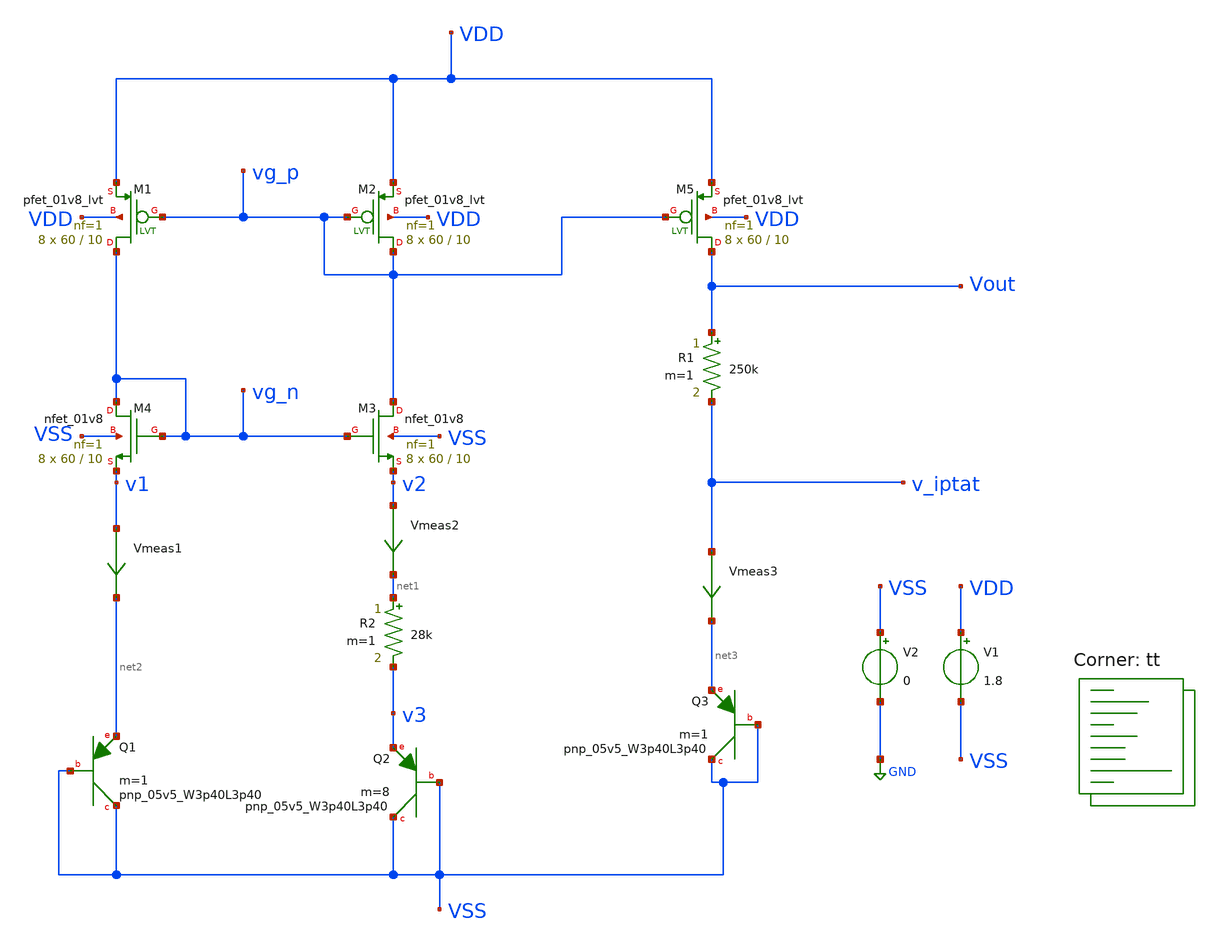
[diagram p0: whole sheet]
** sch_path: xschem/bandgap.sch
**.subckt bandgap
XM4 vg_n vg_n v1 VSS sky130_fd_pr__nfet_01v8 L=10 W=60 nf=1 ad='int((nf+1)/2) * W/nf * 0.29' as='int((nf+2)/2) * W/nf * 0.29'
+ pd='2*int((nf+1)/2) * (W/nf + 0.29)' ps='2*int((nf+2)/2) * (W/nf + 0.29)' nrd='0.29 / W' nrs='0.29 / W'
+ sa=0 sb=0 sd=0 mult=8 m=8
XQ1 VSS VSS net2 sky130_fd_pr__pnp_05v5_W3p40L3p40 m=1
V1 VDD VSS 1.8
XQ3 VSS VSS net3 sky130_fd_pr__pnp_05v5_W3p40L3p40 m=1
R1 Vout v_iptat 250k m=1
XQ2 VSS VSS v3 sky130_fd_pr__pnp_05v5_W3p40L3p40 m=8
R2 net1 v3 28k m=1
V2 VSS GND 0
Vmeas1 v1 net2 0
.save i(vmeas1)
Vmeas2 v2 net1 0
.save i(vmeas2)
Vmeas3 v_iptat net3 0
.save i(vmeas3)
XM1 vg_n vg_p VDD VDD sky130_fd_pr__pfet_01v8_lvt L=10 W=60 nf=1 ad='int((nf+1)/2) * W/nf * 0.29' as='int((nf+2)/2) * W/nf * 0.29'
+ pd='2*int((nf+1)/2) * (W/nf + 0.29)' ps='2*int((nf+2)/2) * (W/nf + 0.29)' nrd='0.29 / W' nrs='0.29 / W'
+ sa=0 sb=0 sd=0 mult=8 m=8
XM2 vg_p vg_p VDD VDD sky130_fd_pr__pfet_01v8_lvt L=10 W=60 nf=1 ad='int((nf+1)/2) * W/nf * 0.29' as='int((nf+2)/2) * W/nf * 0.29'
+ pd='2*int((nf+1)/2) * (W/nf + 0.29)' ps='2*int((nf+2)/2) * (W/nf + 0.29)' nrd='0.29 / W' nrs='0.29 / W'
+ sa=0 sb=0 sd=0 mult=8 m=8
XM3 vg_p vg_n v2 VSS sky130_fd_pr__nfet_01v8 L=10 W=60 nf=1 ad='int((nf+1)/2) * W/nf * 0.29' as='int((nf+2)/2) * W/nf * 0.29'
+ pd='2*int((nf+1)/2) * (W/nf + 0.29)' ps='2*int((nf+2)/2) * (W/nf + 0.29)' nrd='0.29 / W' nrs='0.29 / W'
+ sa=0 sb=0 sd=0 mult=8 m=8
XM5 Vout vg_p VDD VDD sky130_fd_pr__pfet_01v8_lvt L=10 W=60 nf=1 ad='int((nf+1)/2) * W/nf * 0.29' as='int((nf+2)/2) * W/nf * 0.29'
+ pd='2*int((nf+1)/2) * (W/nf + 0.29)' ps='2*int((nf+2)/2) * (W/nf + 0.29)' nrd='0.29 / W' nrs='0.29 / W'
+ sa=0 sb=0 sd=0 mult=8 m=8
**** begin user architecture code
.lib $::SKYWATER_MODELS/sky130.lib.spice tt
**** end user architecture code
**.ends
.GLOBAL GND
**** begin user architecture code


* ngspice commands
.control
save all
save @m.xm1.msky130_fd_pr__pfet_01v8_lvt[vth]
save @m.xm2.msky130_fd_pr__pfet_01v8_lvt[vth]
*dc temp -40 125 0.1
dc V1 1.2 2.5 0.01
plot v(Vout)
*op
write bandgap.raw
.endc



**** end user architecture code
.end
